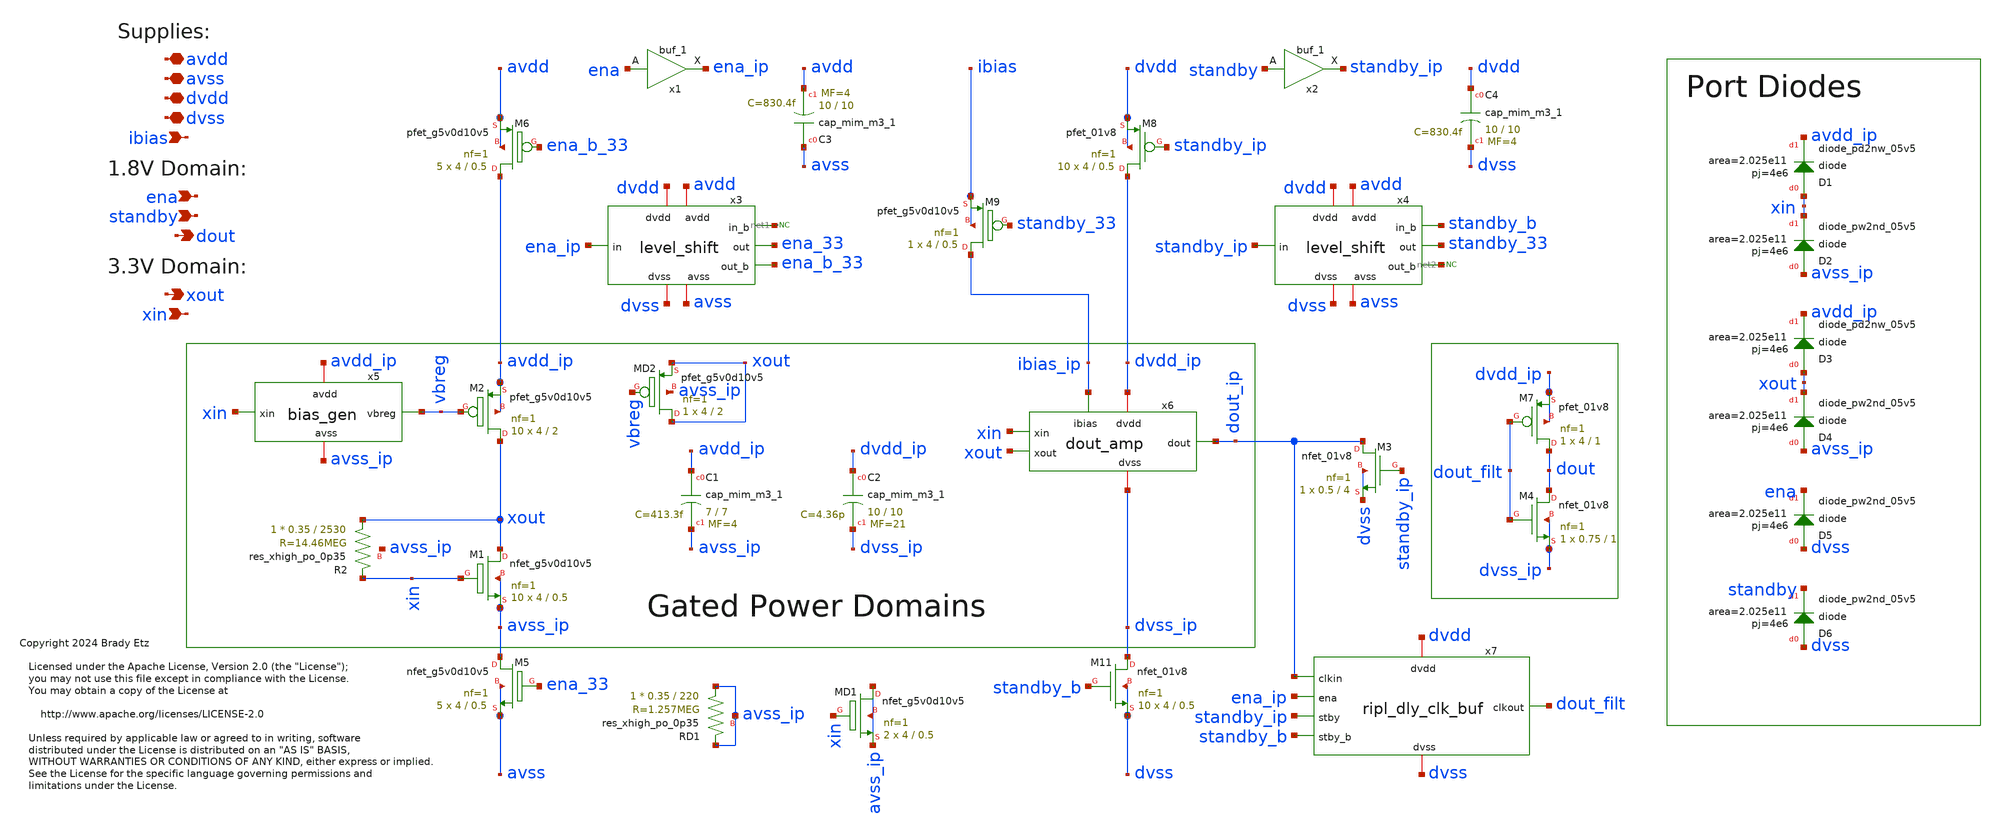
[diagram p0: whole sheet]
** sch_path: xschem/sky130_be_ip__lsxo.sch
* Copyright 2024 Brady Etz
* Licensed under the Apache License, Version 2.0 (the "License");
**.subckt sky130_be_ip__lsxo avdd dout avss dvdd dvss ibias ena standby xin xout
*.iopin avdd
*.opin dout
*.iopin avss
*.iopin dvdd
*.iopin dvss
*.ipin ibias
*.ipin ena
*.ipin standby
*.ipin xin
*.opin xout
XM1 xout xin avss_ip avss_ip sky130_fd_pr__nfet_g5v0d10v5 L=0.5 W=4 nf=1 ad='int((nf+1)/2) * W/nf * 0.29'
+ as='int((nf+2)/2) * W/nf * 0.29' pd='2*int((nf+1)/2) * (W/nf + 0.29)' ps='2*int((nf+2)/2) * (W/nf + 0.29)'
+ nrd='0.29 / W' nrs='0.29 / W' sa=0 sb=0 sd=0 mult=10 m=10
XM2 xout vbreg avdd_ip avdd_ip sky130_fd_pr__pfet_g5v0d10v5 L=2 W=4 nf=1 ad='int((nf+1)/2) * W/nf * 0.29'
+ as='int((nf+2)/2) * W/nf * 0.29' pd='2*int((nf+1)/2) * (W/nf + 0.29)' ps='2*int((nf+2)/2) * (W/nf + 0.29)'
+ nrd='0.29 / W' nrs='0.29 / W' sa=0 sb=0 sd=0 mult=10 m=10
XR2 xout xin avss_ip sky130_fd_pr__res_xhigh_po_0p35 L=2530 mult=1 m=1
XM5 avss_ip ena_33 avss avss sky130_fd_pr__nfet_g5v0d10v5 L=0.5 W=4 nf=1 ad='int((nf+1)/2) * W/nf * 0.29'
+ as='int((nf+2)/2) * W/nf * 0.29' pd='2*int((nf+1)/2) * (W/nf + 0.29)' ps='2*int((nf+2)/2) * (W/nf + 0.29)'
+ nrd='0.29 / W' nrs='0.29 / W' sa=0 sb=0 sd=0 mult=5 m=5
XM6 avdd_ip ena_b_33 avdd avdd sky130_fd_pr__pfet_g5v0d10v5 L=0.5 W=4 nf=1 ad='int((nf+1)/2) * W/nf * 0.29'
+ as='int((nf+2)/2) * W/nf * 0.29' pd='2*int((nf+1)/2) * (W/nf + 0.29)' ps='2*int((nf+2)/2) * (W/nf + 0.29)'
+ nrd='0.29 / W' nrs='0.29 / W' sa=0 sb=0 sd=0 mult=5 m=5
XM8 dvdd_ip standby_ip dvdd dvdd sky130_fd_pr__pfet_01v8 L=0.5 W=4 nf=1 ad='int((nf+1)/2) * W/nf * 0.29'
+ as='int((nf+2)/2) * W/nf * 0.29' pd='2*int((nf+1)/2) * (W/nf + 0.29)' ps='2*int((nf+2)/2) * (W/nf + 0.29)'
+ nrd='0.29 / W' nrs='0.29 / W' sa=0 sb=0 sd=0 mult=10 m=10
XM9 ibias_ip standby_33 ibias ibias sky130_fd_pr__pfet_g5v0d10v5 L=0.5 W=4 nf=1 ad='int((nf+1)/2) * W/nf * 0.29'
+ as='int((nf+2)/2) * W/nf * 0.29' pd='2*int((nf+1)/2) * (W/nf + 0.29)' ps='2*int((nf+2)/2) * (W/nf + 0.29)'
+ nrd='0.29 / W' nrs='0.29 / W' sa=0 sb=0 sd=0 mult=1 m=1
XM11 dvss_ip standby_b dvss dvss sky130_fd_pr__nfet_01v8 L=0.5 W=4 nf=1 ad='int((nf+1)/2) * W/nf * 0.29'
+ as='int((nf+2)/2) * W/nf * 0.29' pd='2*int((nf+1)/2) * (W/nf + 0.29)' ps='2*int((nf+2)/2) * (W/nf + 0.29)'
+ nrd='0.29 / W' nrs='0.29 / W' sa=0 sb=0 sd=0 mult=10 m=10
XC1 avdd_ip avss_ip sky130_fd_pr__cap_mim_m3_1 W=7 L=7 MF=4 m=4
XC2 dvdd_ip dvss_ip sky130_fd_pr__cap_mim_m3_1 W=10 L=10 MF=21 m=21
XC3 avss avdd sky130_fd_pr__cap_mim_m3_1 W=10 L=10 MF=4 m=4
XC4 dvdd dvss sky130_fd_pr__cap_mim_m3_1 W=10 L=10 MF=4 m=4
x7 dvdd dvss dout_ip dout_filt ena_ip standby_ip standby_b ripl_dly_clk_buf
XM3 dout_ip standby_ip dvss dvss sky130_fd_pr__nfet_01v8 L=4 W=0.5 nf=1 ad='int((nf+1)/2) * W/nf * 0.29'
+ as='int((nf+2)/2) * W/nf * 0.29' pd='2*int((nf+1)/2) * (W/nf + 0.29)' ps='2*int((nf+2)/2) * (W/nf + 0.29)'
+ nrd='0.29 / W' nrs='0.29 / W' sa=0 sb=0 sd=0 mult=1 m=1
x3 avdd dvdd ena_33 ena_b_33 ena_ip dvss avss net1 level_shift
x4 avdd dvdd standby_33 net2 standby_ip dvss avss standby_b level_shift
x6 dvdd_ip dvss_ip xin xout ibias_ip dout_ip dout_amp
x5 avdd_ip vbreg xin avss_ip bias_gen
XM4 dout dout_filt dvss_ip dvss_ip sky130_fd_pr__nfet_01v8 L=1 W=0.75 nf=1 ad='int((nf+1)/2) * W/nf * 0.29'
+ as='int((nf+2)/2) * W/nf * 0.29' pd='2*int((nf+1)/2) * (W/nf + 0.29)' ps='2*int((nf+2)/2) * (W/nf + 0.29)'
+ nrd='0.29 / W' nrs='0.29 / W' sa=0 sb=0 sd=0 mult=1 m=1
XM7 dout dout_filt dvdd_ip dvdd_ip sky130_fd_pr__pfet_01v8 L=1 W=4 nf=1 ad='int((nf+1)/2) * W/nf * 0.29'
+ as='int((nf+2)/2) * W/nf * 0.29' pd='2*int((nf+1)/2) * (W/nf + 0.29)' ps='2*int((nf+2)/2) * (W/nf + 0.29)'
+ nrd='0.29 / W' nrs='0.29 / W' sa=0 sb=0 sd=0 mult=1 m=1
x1 ena dvss dvss dvdd dvdd ena_ip sky130_fd_sc_hd__buf_1
x2 standby dvss dvss dvdd dvdd standby_ip sky130_fd_sc_hd__buf_1
* noconn #net1
* noconn #net2
XRD1 avss_ip avss_ip avss_ip sky130_fd_pr__res_xhigh_po_0p35 L=220 mult=1 m=1
XMD1 avss_ip xin avss_ip avss_ip sky130_fd_pr__nfet_g5v0d10v5 L=0.5 W=4 nf=1 ad='int((nf+1)/2) * W/nf * 0.29'
+ as='int((nf+2)/2) * W/nf * 0.29' pd='2*int((nf+1)/2) * (W/nf + 0.29)' ps='2*int((nf+2)/2) * (W/nf + 0.29)'
+ nrd='0.29 / W' nrs='0.29 / W' sa=0 sb=0 sd=0 mult=2 m=2
XD1 xin avdd_ip sky130_fd_pr__diode_pd2nw_05v5 area=2.025e11 pj=4e6
XD2 avss_ip xin sky130_fd_pr__diode_pw2nd_05v5 area=2.025e11 pj=4e6
XD3 xout avdd_ip sky130_fd_pr__diode_pd2nw_05v5 area=2.025e11 pj=4e6
XD4 avss_ip xout sky130_fd_pr__diode_pw2nd_05v5 area=2.025e11 pj=4e6
XD5 dvss ena sky130_fd_pr__diode_pw2nd_05v5 area=2.025e11 pj=4e6
XD6 dvss standby sky130_fd_pr__diode_pw2nd_05v5 area=2.025e11 pj=4e6
XMD2 xout vbreg xout avss_ip sky130_fd_pr__pfet_g5v0d10v5 L=2 W=4 nf=1 ad='int((nf+1)/2) * W/nf * 0.29'
+ as='int((nf+2)/2) * W/nf * 0.29' pd='2*int((nf+1)/2) * (W/nf + 0.29)' ps='2*int((nf+2)/2) * (W/nf + 0.29)'
+ nrd='0.29 / W' nrs='0.29 / W' sa=0 sb=0 sd=0 mult=1 m=1
**.ends
.end
